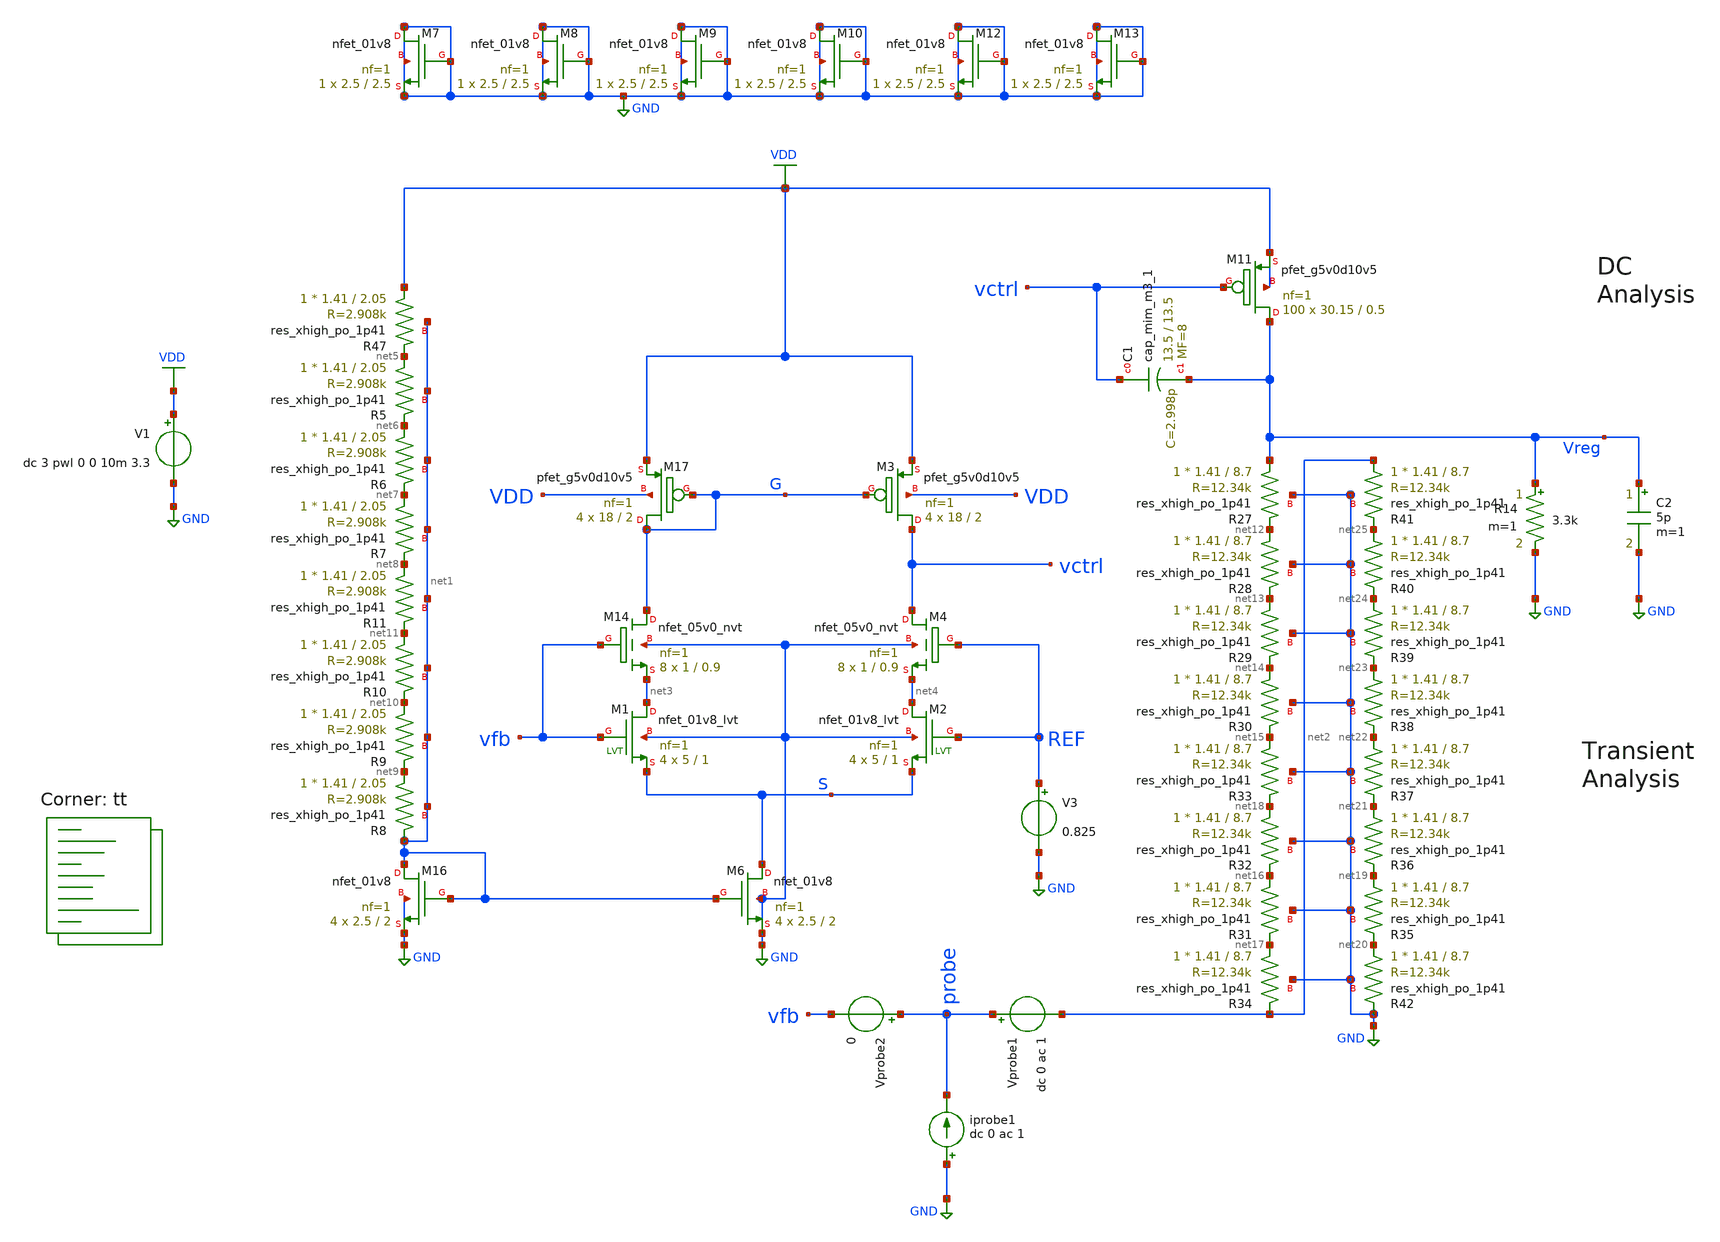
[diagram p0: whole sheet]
** sch_path: ALDO/Schematic/Testbenches/LDO4_stef_stb.sch
**.subckt LDO4_stef_stb
V1 VDD GND dc 3 pwl 0 0 10m 3.3
XM11 Vreg vctrl VDD VDD sky130_fd_pr__pfet_g5v0d10v5 L=0.5 W=30.15 nf=1 ad='int((nf+1)/2) * W/nf * 0.29'
+ as='int((nf+2)/2) * W/nf * 0.29' pd='2*int((nf+1)/2) * (W/nf + 0.29)' ps='2*int((nf+2)/2) * (W/nf + 0.29)'
+ nrd='0.29 / W' nrs='0.29 / W' sa=0 sb=0 sd=0 mult=100 m=100
V3 REF GND 0.825
C2 Vreg GND 5p m=1
R14 Vreg GND 3.3k m=1
XM16 net1 net1 GND GND sky130_fd_pr__nfet_01v8 L=2 W=2.5 nf=1 ad='int((nf+1)/2) * W/nf * 0.29' as='int((nf+2)/2) * W/nf * 0.29'
+ pd='2*int((nf+1)/2) * (W/nf + 0.29)' ps='2*int((nf+2)/2) * (W/nf + 0.29)' nrd='0.29 / W' nrs='0.29 / W'
+ sa=0 sb=0 sd=0 mult=4 m=4
XM6 S net1 GND GND sky130_fd_pr__nfet_01v8 L=2 W=2.5 nf=1 ad='int((nf+1)/2) * W/nf * 0.29' as='int((nf+2)/2) * W/nf * 0.29'
+ pd='2*int((nf+1)/2) * (W/nf + 0.29)' ps='2*int((nf+2)/2) * (W/nf + 0.29)' nrd='0.29 / W' nrs='0.29 / W'
+ sa=0 sb=0 sd=0 mult=4 m=4
XM3 vctrl G VDD VDD sky130_fd_pr__pfet_g5v0d10v5 L=2 W=18 nf=1 ad='int((nf+1)/2) * W/nf * 0.29' as='int((nf+2)/2) * W/nf * 0.29'
+ pd='2*int((nf+1)/2) * (W/nf + 0.29)' ps='2*int((nf+2)/2) * (W/nf + 0.29)' nrd='0.29 / W' nrs='0.29 / W'
+ sa=0 sb=0 sd=0 mult=4 m=4
XM17 G G VDD VDD sky130_fd_pr__pfet_g5v0d10v5 L=2 W=18 nf=1 ad='int((nf+1)/2) * W/nf * 0.29' as='int((nf+2)/2) * W/nf * 0.29'
+ pd='2*int((nf+1)/2) * (W/nf + 0.29)' ps='2*int((nf+2)/2) * (W/nf + 0.29)' nrd='0.29 / W' nrs='0.29 / W'
+ sa=0 sb=0 sd=0 mult=4 m=4
XM7 GND GND GND GND sky130_fd_pr__nfet_01v8 L=2.5 W=2.5 nf=1 ad='int((nf+1)/2) * W/nf * 0.29' as='int((nf+2)/2) * W/nf * 0.29'
+ pd='2*int((nf+1)/2) * (W/nf + 0.29)' ps='2*int((nf+2)/2) * (W/nf + 0.29)' nrd='0.29 / W' nrs='0.29 / W'
+ sa=0 sb=0 sd=0 mult=1 m=1
XM8 GND GND GND GND sky130_fd_pr__nfet_01v8 L=2.5 W=2.5 nf=1 ad='int((nf+1)/2) * W/nf * 0.29' as='int((nf+2)/2) * W/nf * 0.29'
+ pd='2*int((nf+1)/2) * (W/nf + 0.29)' ps='2*int((nf+2)/2) * (W/nf + 0.29)' nrd='0.29 / W' nrs='0.29 / W'
+ sa=0 sb=0 sd=0 mult=1 m=1
XM9 GND GND GND GND sky130_fd_pr__nfet_01v8 L=2.5 W=2.5 nf=1 ad='int((nf+1)/2) * W/nf * 0.29' as='int((nf+2)/2) * W/nf * 0.29'
+ pd='2*int((nf+1)/2) * (W/nf + 0.29)' ps='2*int((nf+2)/2) * (W/nf + 0.29)' nrd='0.29 / W' nrs='0.29 / W'
+ sa=0 sb=0 sd=0 mult=1 m=1
XM10 GND GND GND GND sky130_fd_pr__nfet_01v8 L=2.5 W=2.5 nf=1 ad='int((nf+1)/2) * W/nf * 0.29' as='int((nf+2)/2) * W/nf * 0.29'
+ pd='2*int((nf+1)/2) * (W/nf + 0.29)' ps='2*int((nf+2)/2) * (W/nf + 0.29)' nrd='0.29 / W' nrs='0.29 / W'
+ sa=0 sb=0 sd=0 mult=1 m=1
XM12 GND GND GND GND sky130_fd_pr__nfet_01v8 L=2.5 W=2.5 nf=1 ad='int((nf+1)/2) * W/nf * 0.29' as='int((nf+2)/2) * W/nf * 0.29'
+ pd='2*int((nf+1)/2) * (W/nf + 0.29)' ps='2*int((nf+2)/2) * (W/nf + 0.29)' nrd='0.29 / W' nrs='0.29 / W'
+ sa=0 sb=0 sd=0 mult=1 m=1
XM13 GND GND GND GND sky130_fd_pr__nfet_01v8 L=2.5 W=2.5 nf=1 ad='int((nf+1)/2) * W/nf * 0.29' as='int((nf+2)/2) * W/nf * 0.29'
+ pd='2*int((nf+1)/2) * (W/nf + 0.29)' ps='2*int((nf+2)/2) * (W/nf + 0.29)' nrd='0.29 / W' nrs='0.29 / W'
+ sa=0 sb=0 sd=0 mult=1 m=1
XM1 net3 vfb S GND sky130_fd_pr__nfet_01v8_lvt L=1 W=5 nf=1 ad='int((nf+1)/2) * W/nf * 0.29' as='int((nf+2)/2) * W/nf * 0.29'
+ pd='2*int((nf+1)/2) * (W/nf + 0.29)' ps='2*int((nf+2)/2) * (W/nf + 0.29)' nrd='0.29 / W' nrs='0.29 / W'
+ sa=0 sb=0 sd=0 mult=4 m=4
XM2 net4 REF S GND sky130_fd_pr__nfet_01v8_lvt L=1 W=5 nf=1 ad='int((nf+1)/2) * W/nf * 0.29' as='int((nf+2)/2) * W/nf * 0.29'
+ pd='2*int((nf+1)/2) * (W/nf + 0.29)' ps='2*int((nf+2)/2) * (W/nf + 0.29)' nrd='0.29 / W' nrs='0.29 / W'
+ sa=0 sb=0 sd=0 mult=4 m=4
XR47 VDD net5 net1 sky130_fd_pr__res_xhigh_po_1p41 L=2.05 mult=1 m=1
XR5 net5 net6 net1 sky130_fd_pr__res_xhigh_po_1p41 L=2.05 mult=1 m=1
XR6 net6 net7 net1 sky130_fd_pr__res_xhigh_po_1p41 L=2.05 mult=1 m=1
XR7 net7 net8 net1 sky130_fd_pr__res_xhigh_po_1p41 L=2.05 mult=1 m=1
XR8 net9 net1 net1 sky130_fd_pr__res_xhigh_po_1p41 L=2.05 mult=1 m=1
XR9 net10 net9 net1 sky130_fd_pr__res_xhigh_po_1p41 L=2.05 mult=1 m=1
XR10 net11 net10 net1 sky130_fd_pr__res_xhigh_po_1p41 L=2.05 mult=1 m=1
XR11 net8 net11 net1 sky130_fd_pr__res_xhigh_po_1p41 L=2.05 mult=1 m=1
XR27 Vreg net12 GND sky130_fd_pr__res_xhigh_po_1p41 L=8.7 mult=1 m=1
XR28 net12 net13 GND sky130_fd_pr__res_xhigh_po_1p41 L=8.7 mult=1 m=1
XR29 net13 net14 GND sky130_fd_pr__res_xhigh_po_1p41 L=8.7 mult=1 m=1
XR30 net14 net15 GND sky130_fd_pr__res_xhigh_po_1p41 L=8.7 mult=1 m=1
XR31 net16 net17 GND sky130_fd_pr__res_xhigh_po_1p41 L=8.7 mult=1 m=1
XR32 net18 net16 GND sky130_fd_pr__res_xhigh_po_1p41 L=8.7 mult=1 m=1
XR33 net15 net18 GND sky130_fd_pr__res_xhigh_po_1p41 L=8.7 mult=1 m=1
XR34 net17 net2 GND sky130_fd_pr__res_xhigh_po_1p41 L=8.7 mult=1 m=1
XR35 net19 net20 GND sky130_fd_pr__res_xhigh_po_1p41 L=8.7 mult=1 m=1
XR36 net21 net19 GND sky130_fd_pr__res_xhigh_po_1p41 L=8.7 mult=1 m=1
XR37 net22 net21 GND sky130_fd_pr__res_xhigh_po_1p41 L=8.7 mult=1 m=1
XR38 net23 net22 GND sky130_fd_pr__res_xhigh_po_1p41 L=8.7 mult=1 m=1
XR39 net24 net23 GND sky130_fd_pr__res_xhigh_po_1p41 L=8.7 mult=1 m=1
XR40 net25 net24 GND sky130_fd_pr__res_xhigh_po_1p41 L=8.7 mult=1 m=1
XR41 net2 net25 GND sky130_fd_pr__res_xhigh_po_1p41 L=8.7 mult=1 m=1
XR42 net20 GND GND sky130_fd_pr__res_xhigh_po_1p41 L=8.7 mult=1 m=1
Vprobe2 probe vfb 0
Vprobe1 probe net2 dc 0 ac 1
iprobe1 GND probe dc 0 ac 1
XC1 vctrl Vreg sky130_fd_pr__cap_mim_m3_1 W=13.5 L=13.5 MF=8 m=8
XM14 G vfb net3 GND sky130_fd_pr__nfet_05v0_nvt L=0.9 W=1 nf=1 ad='int((nf+1)/2) * W/nf * 0.29' as='int((nf+2)/2) * W/nf * 0.29'
+ pd='2*int((nf+1)/2) * (W/nf + 0.29)' ps='2*int((nf+2)/2) * (W/nf + 0.29)' nrd='0.29 / W' nrs='0.29 / W'
+ sa=0 sb=0 sd=0 mult=8 m=8
XM4 vctrl REF net4 GND sky130_fd_pr__nfet_05v0_nvt L=0.9 W=1 nf=1 ad='int((nf+1)/2) * W/nf * 0.29' as='int((nf+2)/2) * W/nf * 0.29'
+ pd='2*int((nf+1)/2) * (W/nf + 0.29)' ps='2*int((nf+2)/2) * (W/nf + 0.29)' nrd='0.29 / W' nrs='0.29 / W'
+ sa=0 sb=0 sd=0 mult=8 m=8
**** begin user architecture code
.lib $::SKYWATER_MODELS/sky130.lib.spice tt


.options savecurrents
.control
 let runs=2
 let run=0

 alter @Vprobe1[acmag]=1
 alter @iprobe1[acmag]=0

 dowhile run < runs

 set run =$&run
 ac dec 20 0.01 10G
 write OTA_STB_TB_{$run}.raw

 all
 alter @Vprobe1[acmag]=0
 alter @iprobe1[acmag]=1
 let run = run + 1
 end

 let ip22 = ac2.i(Vprobe2)
 let vprb1 = ac1.probe
 let mb = 1/(vprb1+ip22)-1
 let phase_mb = 180/PI*vp(mb)
 plot vdb(mb)
 plot phase_mb
 plot vdb(mb) phase_mb
 write /foss/designs/OTA-tt.txt vdb(mb) phase_mb

 meas ac peak MAX vmag(mb) FROM=2 TO=1.5G
 let f3db = peak/sqrt(2)
 meas ac f1 WHEN vmag(mb)=f3db RISE=1
 meas ac BW WHEN vmag(mb)=f3db FALL=1
 let GBW = peak*BW
 meas ac pm_deg find phase_mb when vdb(mb)=0
 meas ac dominant_pole_f when vdb(mb)=0
 meas ac loop_gain find vdb(mb) at=0.01
 let Phase_margin=180-abs(pm_deg)
 print GBW
 print Phase_margin

 op
 show m : gm : gmbs : gds : vds : vdsat : vgs : vth : id : cgg
.endc

**** end user architecture code
**.ends
.GLOBAL VDD
.GLOBAL GND
.end
